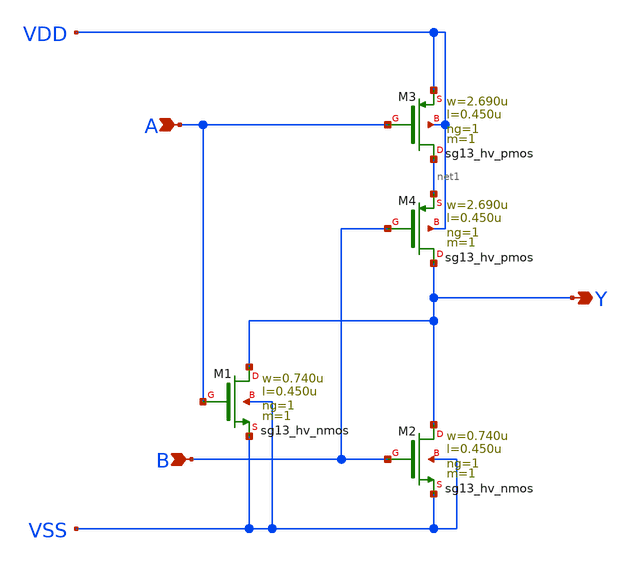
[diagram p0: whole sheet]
** sch_path: ihp-sg13g2/libs.ref/sg13g2_stdcell_hv/sch/xschem/sg13g2_hv_nor2_1.sch
* Copyright 2023 IHP PDK Authors
* Licensed under the Apache License, Version 2.0 (the "License");
* you may not use this file except in compliance with the License.
* You may obtain a copy of the License at
* https://www.apache.org/licenses/LICENSE-2.0
* Unless required by applicable law or agreed to in writing, software
* distributed under the License is distributed on an "AS IS" BASIS,
* WITHOUT WARRANTIES OR CONDITIONS OF ANY KIND, either express or implied.
* See the License for the specific language governing permissions and
* limitations under the License.
**.subckt sg13g2_hv_nor2_1 Y B A
*.opin Y
*.ipin B
*.ipin A
XM1 Y A VSS VSS sg13_hv_nmos w=0.740u l=0.450u ng=1 m=1 mm_ok=1
XM2 Y B VSS VSS sg13_hv_nmos w=0.740u l=0.450u ng=1 m=1 mm_ok=1
XM3 net1 A VDD VDD sg13_hv_pmos w=2.690u l=0.450u ng=1 m=1 mm_ok=1
XM4 Y B net1 VDD sg13_hv_pmos w=2.690u l=0.450u ng=1 m=1 mm_ok=1
**.ends
.end
